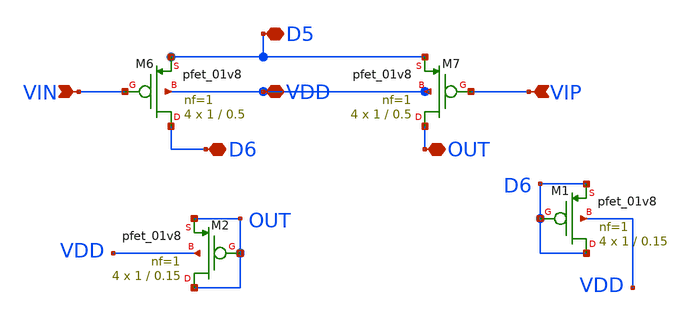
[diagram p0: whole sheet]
** sch_path: opamp/mag/pmos67/pmos67.sch
**.subckt pmos67 VDD D5 VIN VIP OUT D6
*.iopin VDD
*.iopin D5
*.ipin VIN
*.ipin VIP
*.iopin OUT
*.iopin D6
XM6 D6 VIN D5 VDD sky130_fd_pr__pfet_01v8 L=0.5 W=1 nf=1 ad='int((nf+1)/2) * W/nf * 0.29' as='int((nf+2)/2) * W/nf * 0.29'
+ pd='2*int((nf+1)/2) * (W/nf + 0.29)' ps='2*int((nf+2)/2) * (W/nf + 0.29)' nrd='0.29 / W' nrs='0.29 / W'
+ sa=0 sb=0 sd=0 mult=4 m=4
XM7 OUT VIP D5 VDD sky130_fd_pr__pfet_01v8 L=0.5 W=1 nf=1 ad='int((nf+1)/2) * W/nf * 0.29' as='int((nf+2)/2) * W/nf * 0.29'
+ pd='2*int((nf+1)/2) * (W/nf + 0.29)' ps='2*int((nf+2)/2) * (W/nf + 0.29)' nrd='0.29 / W' nrs='0.29 / W'
+ sa=0 sb=0 sd=0 mult=4 m=4
XM1 D6 D6 D6 VDD sky130_fd_pr__pfet_01v8 L=0.15 W=1 nf=1 ad='int((nf+1)/2) * W/nf * 0.29' as='int((nf+2)/2) * W/nf * 0.29'
+ pd='2*int((nf+1)/2) * (W/nf + 0.29)' ps='2*int((nf+2)/2) * (W/nf + 0.29)' nrd='0.29 / W' nrs='0.29 / W'
+ sa=0 sb=0 sd=0 mult=4 m=4
XM2 OUT OUT OUT VDD sky130_fd_pr__pfet_01v8 L=0.15 W=1 nf=1 ad='int((nf+1)/2) * W/nf * 0.29' as='int((nf+2)/2) * W/nf * 0.29'
+ pd='2*int((nf+1)/2) * (W/nf + 0.29)' ps='2*int((nf+2)/2) * (W/nf + 0.29)' nrd='0.29 / W' nrs='0.29 / W'
+ sa=0 sb=0 sd=0 mult=4 m=4
**.ends
.end
